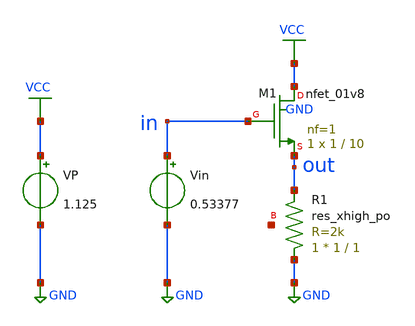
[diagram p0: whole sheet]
** sch_path: Amplifier_Inv/xschem/v2/find_subthresh.sch
**.subckt find_subthresh
Vin in GND 0.53377
XM1 VCC in out GND sky130_fd_pr__nfet_01v8 L=10 W=1 nf=1 ad='int((nf+1)/2) * W/nf * 0.29' as='int((nf+2)/2) * W/nf * 0.29'
+ pd='2*int((nf+1)/2) * (W/nf + 0.29)' ps='2*int((nf+2)/2) * (W/nf + 0.29)' nrd='0.29 / W' nrs='0.29 / W'
+ sa=0 sb=0 sd=0 mult=1 m=1
VP VCC GND 1.125
XR1 GND out net1 sky130_fd_pr__res_xhigh_po W=1 L=1 mult=1 m=1
**** begin user architecture code

.control

  dc Vin 0 1.125 0.00001
  save all v(out) v(in)
  write tb_inv_sky130_a_DC_v2.raw v(out) v(in)

.endc



** opencircuitdesign pdks install
.lib $::SKYWATER_MODELS/sky130.lib.spice tt


**** end user architecture code
**.ends
.GLOBAL GND
.GLOBAL VCC
.end
